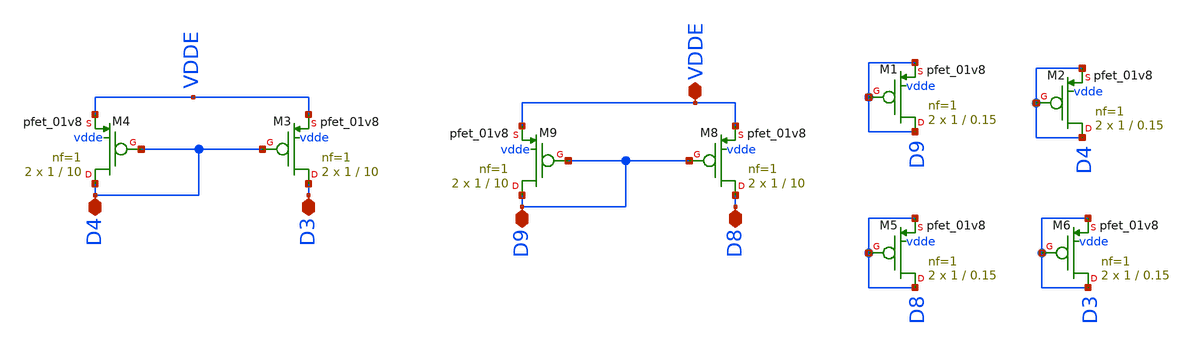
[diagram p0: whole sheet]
** sch_path: magic/pmos_current_bgr_2.sch
**.subckt pmos_current_bgr_2 VDDE D4 D3 D9 D8
*.iopin VDDE
*.iopin D4
*.iopin D3
*.iopin D9
*.iopin D8
XM8 D8 D9 VDDE vdde sky130_fd_pr__pfet_01v8 L=10 W=1 nf=1 ad='int((nf+1)/2) * W/nf * 0.29' as='int((nf+2)/2) * W/nf * 0.29'
+ pd='2*int((nf+1)/2) * (W/nf + 0.29)' ps='2*int((nf+2)/2) * (W/nf + 0.29)' nrd='0.29 / W' nrs='0.29 / W'
+ sa=0 sb=0 sd=0 mult=2 m=2
XM9 D9 D9 VDDE vdde sky130_fd_pr__pfet_01v8 L=10 W=1 nf=1 ad='int((nf+1)/2) * W/nf * 0.29' as='int((nf+2)/2) * W/nf * 0.29'
+ pd='2*int((nf+1)/2) * (W/nf + 0.29)' ps='2*int((nf+2)/2) * (W/nf + 0.29)' nrd='0.29 / W' nrs='0.29 / W'
+ sa=0 sb=0 sd=0 mult=2 m=2
XM3 D3 D4 VDDE vdde sky130_fd_pr__pfet_01v8 L=10 W=1 nf=1 ad='int((nf+1)/2) * W/nf * 0.29' as='int((nf+2)/2) * W/nf * 0.29'
+ pd='2*int((nf+1)/2) * (W/nf + 0.29)' ps='2*int((nf+2)/2) * (W/nf + 0.29)' nrd='0.29 / W' nrs='0.29 / W'
+ sa=0 sb=0 sd=0 mult=2 m=2
XM4 D4 D4 VDDE vdde sky130_fd_pr__pfet_01v8 L=10 W=1 nf=1 ad='int((nf+1)/2) * W/nf * 0.29' as='int((nf+2)/2) * W/nf * 0.29'
+ pd='2*int((nf+1)/2) * (W/nf + 0.29)' ps='2*int((nf+2)/2) * (W/nf + 0.29)' nrd='0.29 / W' nrs='0.29 / W'
+ sa=0 sb=0 sd=0 mult=2 m=2
XM1 D9 D9 D9 vdde sky130_fd_pr__pfet_01v8 L=0.15 W=1 nf=1 ad='int((nf+1)/2) * W/nf * 0.29' as='int((nf+2)/2) * W/nf * 0.29'
+ pd='2*int((nf+1)/2) * (W/nf + 0.29)' ps='2*int((nf+2)/2) * (W/nf + 0.29)' nrd='0.29 / W' nrs='0.29 / W'
+ sa=0 sb=0 sd=0 mult=2 m=2
XM2 D4 D4 D4 vdde sky130_fd_pr__pfet_01v8 L=0.15 W=1 nf=1 ad='int((nf+1)/2) * W/nf * 0.29' as='int((nf+2)/2) * W/nf * 0.29'
+ pd='2*int((nf+1)/2) * (W/nf + 0.29)' ps='2*int((nf+2)/2) * (W/nf + 0.29)' nrd='0.29 / W' nrs='0.29 / W'
+ sa=0 sb=0 sd=0 mult=2 m=2
XM5 D8 D8 D8 vdde sky130_fd_pr__pfet_01v8 L=0.15 W=1 nf=1 ad='int((nf+1)/2) * W/nf * 0.29' as='int((nf+2)/2) * W/nf * 0.29'
+ pd='2*int((nf+1)/2) * (W/nf + 0.29)' ps='2*int((nf+2)/2) * (W/nf + 0.29)' nrd='0.29 / W' nrs='0.29 / W'
+ sa=0 sb=0 sd=0 mult=2 m=2
XM6 D3 D3 D3 vdde sky130_fd_pr__pfet_01v8 L=0.15 W=1 nf=1 ad='int((nf+1)/2) * W/nf * 0.29' as='int((nf+2)/2) * W/nf * 0.29'
+ pd='2*int((nf+1)/2) * (W/nf + 0.29)' ps='2*int((nf+2)/2) * (W/nf + 0.29)' nrd='0.29 / W' nrs='0.29 / W'
+ sa=0 sb=0 sd=0 mult=2 m=2
**.ends
.end
